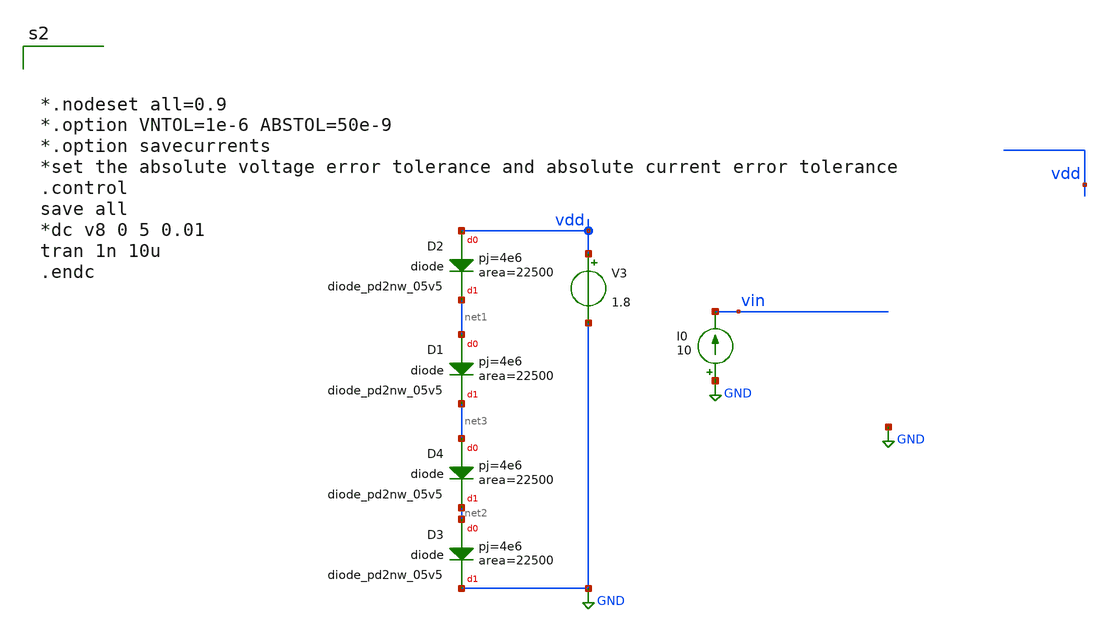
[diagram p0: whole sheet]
** sch_path: xschem/src/diode.sch
**.subckt diode
V3 vdd GND 1.8
I0 GND vin 10
XD4 net3 net2 sky130_fd_pr__diode_pd2nw_05v5 area=22500 pj=4e6
XD1 net1 net3 sky130_fd_pr__diode_pd2nw_05v5 area=22500 pj=4e6
XD2 vdd net1 sky130_fd_pr__diode_pd2nw_05v5 area=22500 pj=4e6
XD3 net2 GND sky130_fd_pr__diode_pd2nw_05v5 area=22500 pj=4e6
**** begin user architecture code



*.nodeset all=0.9
*.option VNTOL=1e-6 ABSTOL=50e-9
*.option savecurrents
*set the absolute voltage error tolerance and absolute current error tolerance
.control
save all
*dc v8 0 5 0.01
tran 1n 10u
.endc





.include /home/eda/pdk/skywater-pdk/libraries/sky130_fd_pr_ngspice/latest/cells/diode_pd2nw_05v5/sky130_fd_pr__diode_pd2nw_05v5.model.spice
.include /home/eda/pdk/skywater-pdk/libraries/sky130_fd_pr_ngspice/latest/cells/diode_pw2nd_05v5/sky130_fd_pr__diode_pw2nd_05v5.model.spice
*.include /home/eda/pdk/skywater-pdk/libraries/sky130_fd_pr_ngspice/latest/models/corners/tt.spice


* Resistor$::SKYWATER_MODELS/Capacitor
.include $::SKYWATER_MODELS/models/r+c/res_typical__cap_typical.spice
.include $::SKYWATER_MODELS/models/r+c/res_typical__cap_typical__lin.spice
* Special cells
.include $::SKYWATER_MODELS/models/corners/tt/specialized_cells.spice


**** end user architecture code
**.ends
.GLOBAL GND
.end
